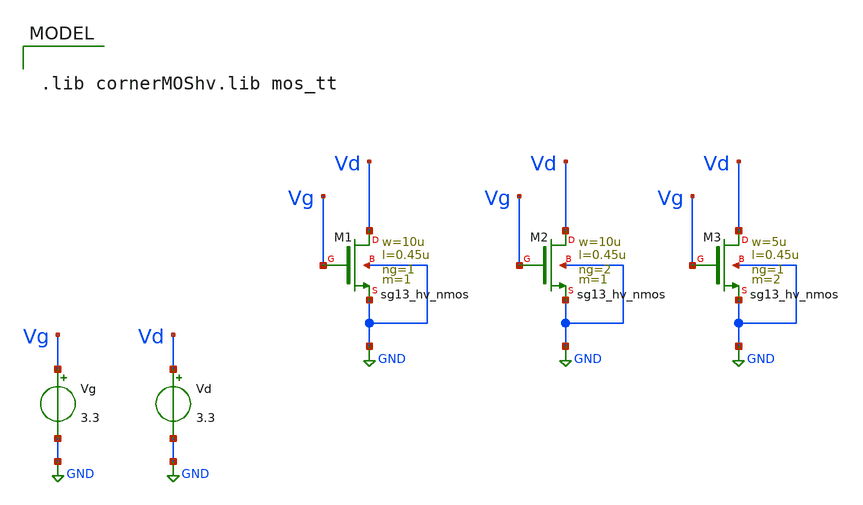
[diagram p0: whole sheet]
** sch_path: xschem/CMOS_Char/Vgs_HvMOS.sch
**.subckt Vgs_HvMOS
XM1 Vd Vg GND GND sg13_hv_nmos w=10u l=0.45u ng=1 m=1 mm_ok=1
Vg Vg GND 3.3
Vd Vd GND 3.3
XM2 Vd Vg GND GND sg13_hv_nmos w=10u l=0.45u ng=2 m=1 mm_ok=1
XM3 Vd Vg GND GND sg13_hv_nmos w=5u l=0.45u ng=1 m=2 mm_ok=1
**** begin user architecture code



.control

*** ALMACENAR DATOS Y CORRER SIMULACION

save all  @n.xm1.nsg13_hv_nmos[vgs]  @n.xm1.nsg13_hv_nmos[ids]  @n.xm1.nsg13_hv_nmos[gm]
+  @n.xm1.nsg13_hv_nmos[vth]  @n.xm2.nsg13_hv_nmos[vgs]  @n.xm2.nsg13_hv_nmos[ids]  @n.xm2.nsg13_hv_nmos[gm]
+  @n.xm2.nsg13_hv_nmos[vth]  @n.xm3.nsg13_hv_nmos[vgs]  @n.xm3.nsg13_hv_nmos[ids]  @n.xm3.nsg13_hv_nmos[gm]
+  @n.xm3.nsg13_hv_nmos[vth]

dc Vg 0 3.3 0.01

*** GUARDAR DATOS COMO VARIABLES Y GRAFICAR

let vgs1 = @n.xm1.nsg13_hv_nmos[vgs]
let ids1 = @n.xm1.nsg13_hv_nmos[ids]
let gm1 = @n.xm1.nsg13_hv_nmos[gm]
let vth1 = @n.xm1.nsg13_hv_nmos[vth]

let vgs2 = @n.xm2.nsg13_hv_nmos[vgs]
let ids2 = @n.xm2.nsg13_hv_nmos[ids]
let gm1 = @n.xm2.nsg13_hv_nmos[gm]
let vth2 = @n.xm2.nsg13_hv_nmos[vth]


let vgs3 = @n.xm3.nsg13_hv_nmos[vgs]
let ids3 = @n.xm3.nsg13_hv_nmos[ids]
let gm3 = @n.xm3.nsg13_hv_nmos[gm]
let vth3 = @n.xm3.nsg13_hv_nmos[vth]

plot ids1 vs vgs1
plot ids2 vs vgs2
plot ids3 vs vgs3

print ids1[330]
print ids2[330]
print ids3[330]

*plot gm1 vs vgs1
*plot gm2 vs vgs2
*plot gm3 vs vgs3
.endc



.lib cornerMOShv.lib mos_tt

**** end user architecture code
**.ends
.GLOBAL GND
.end
